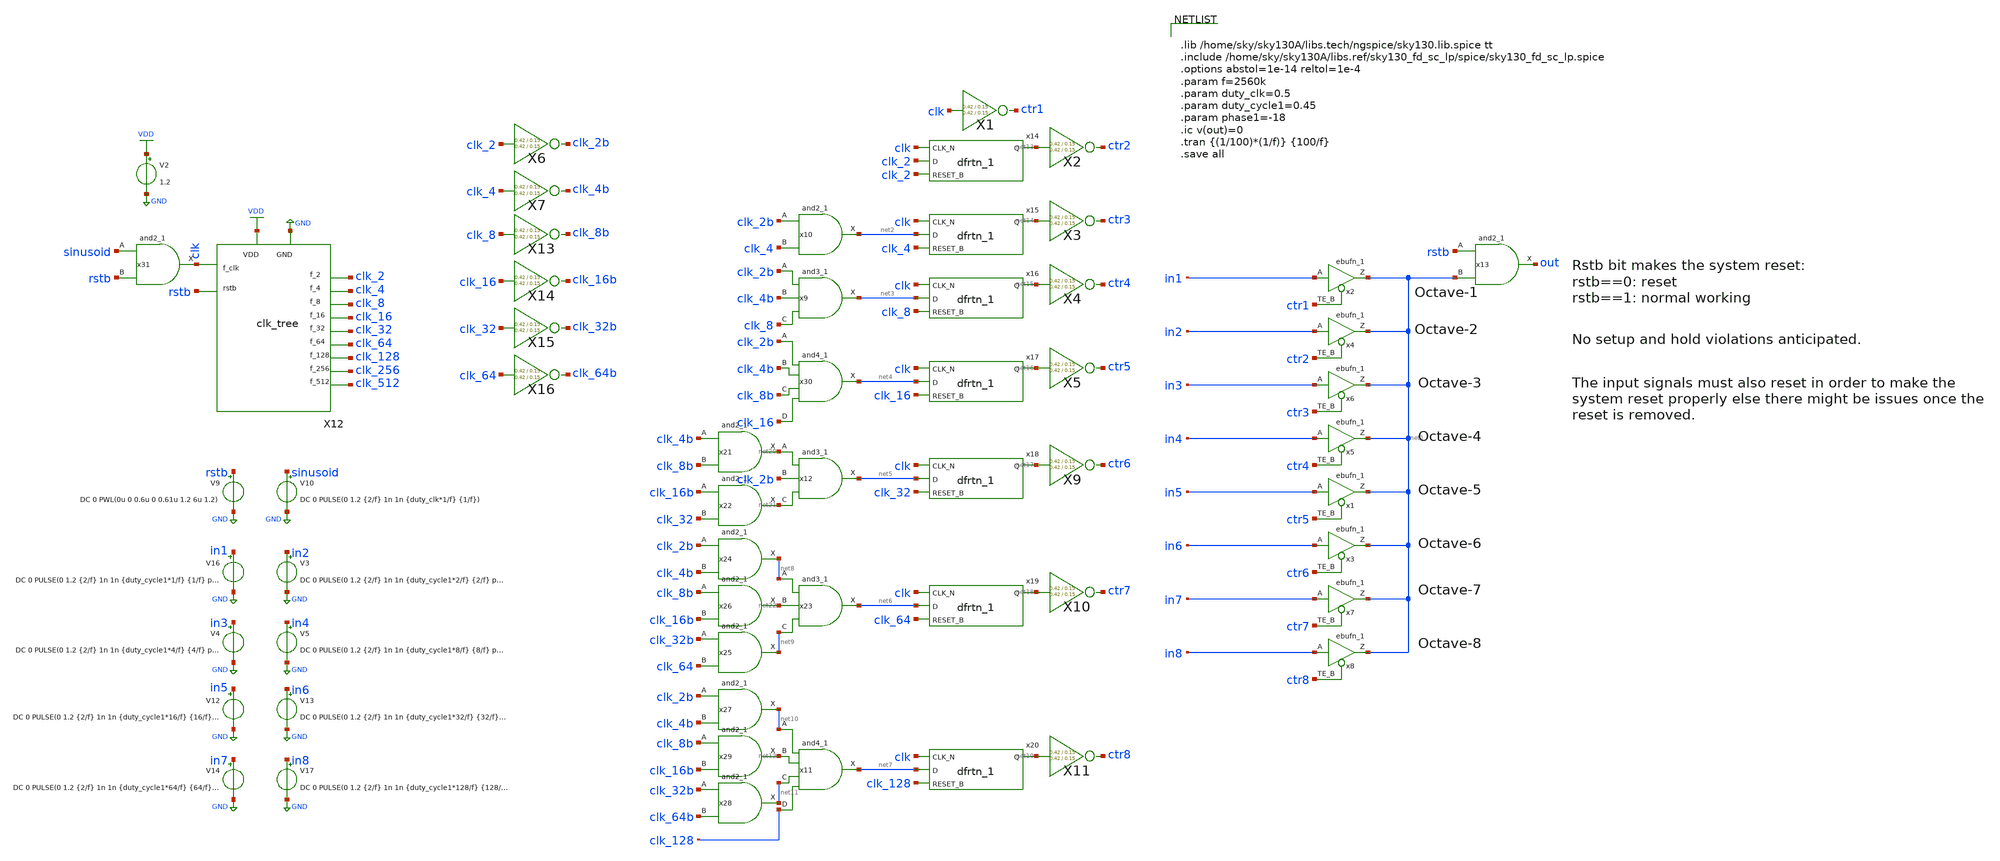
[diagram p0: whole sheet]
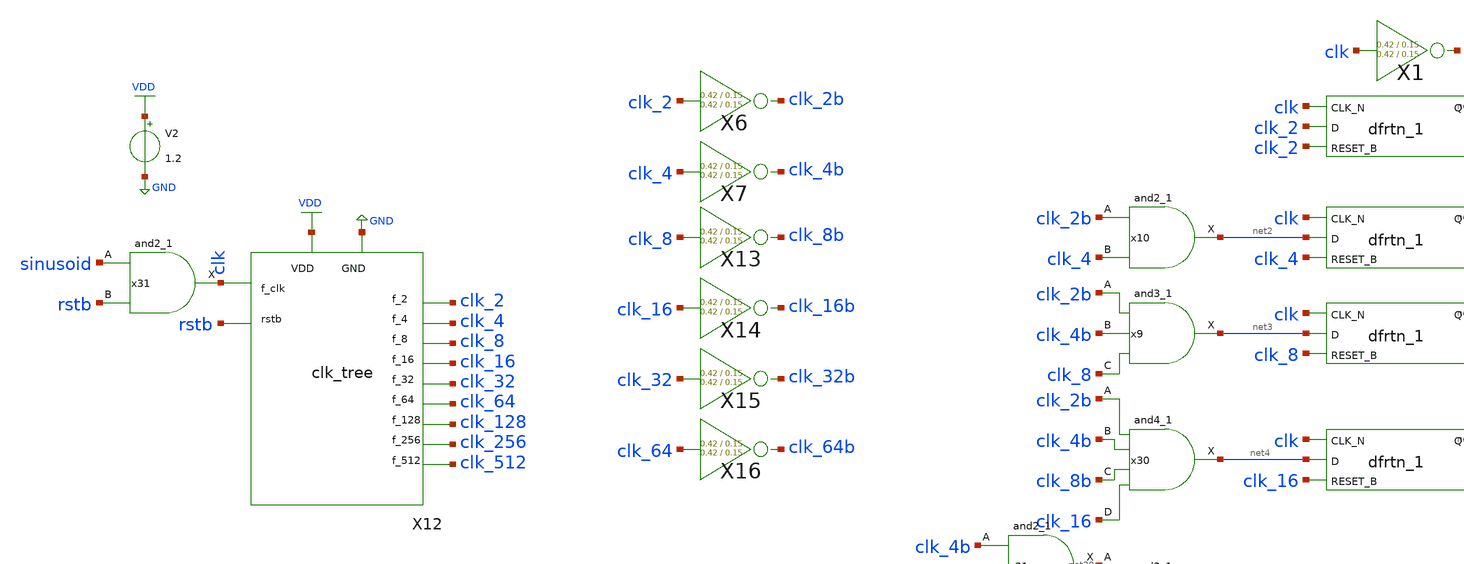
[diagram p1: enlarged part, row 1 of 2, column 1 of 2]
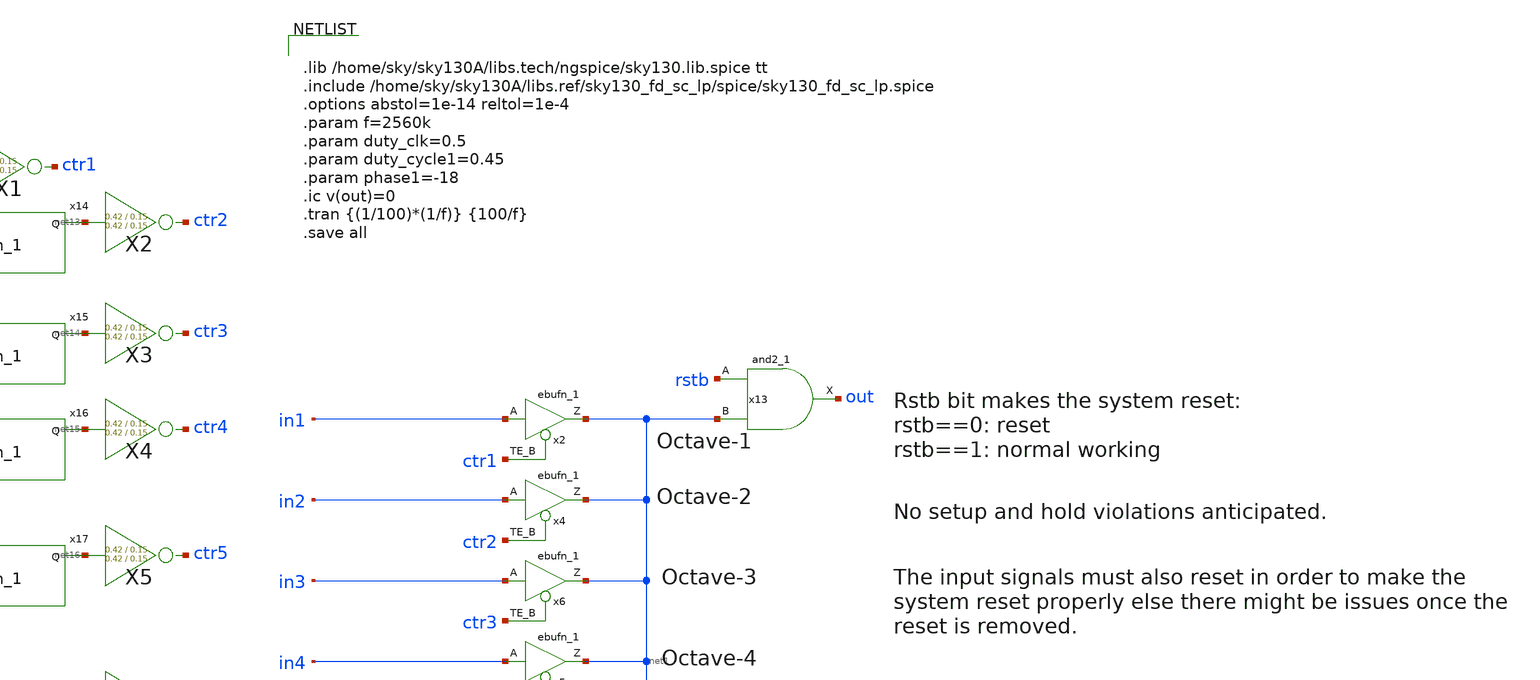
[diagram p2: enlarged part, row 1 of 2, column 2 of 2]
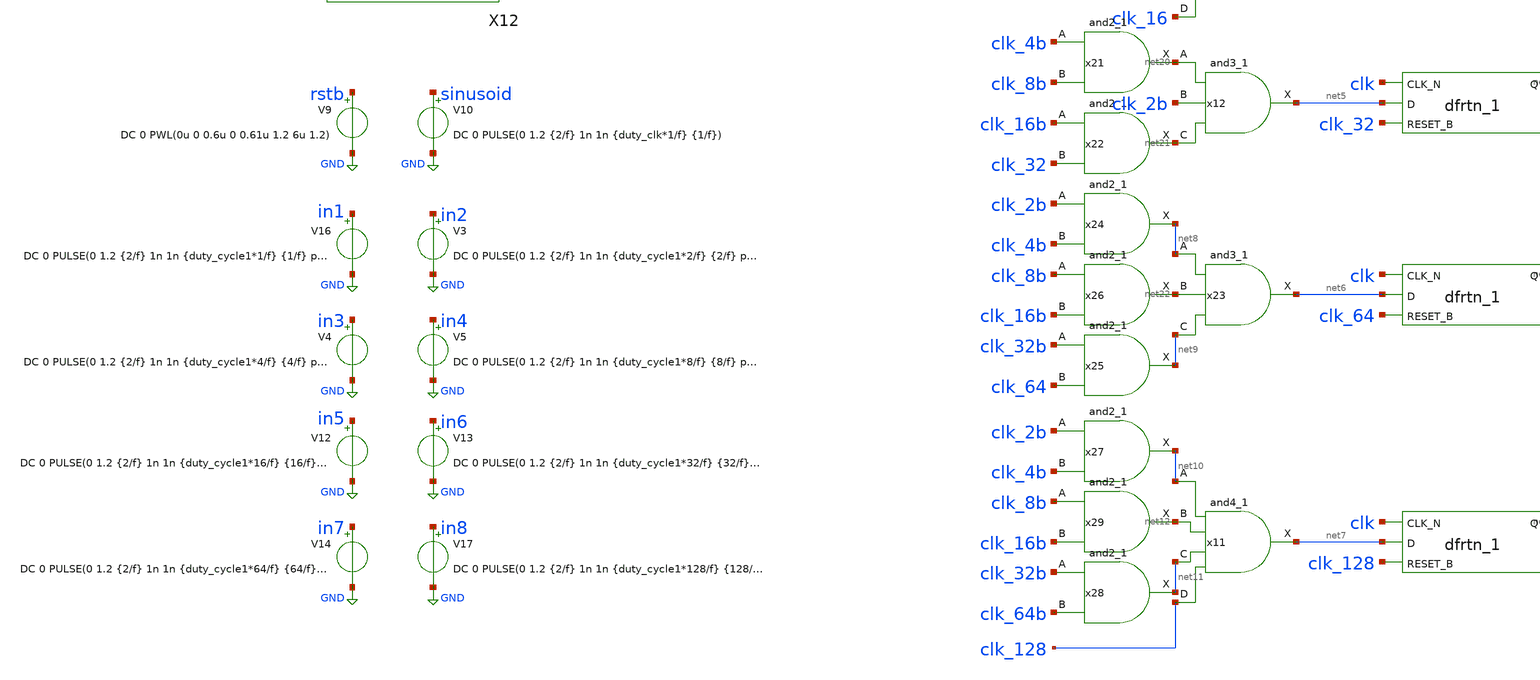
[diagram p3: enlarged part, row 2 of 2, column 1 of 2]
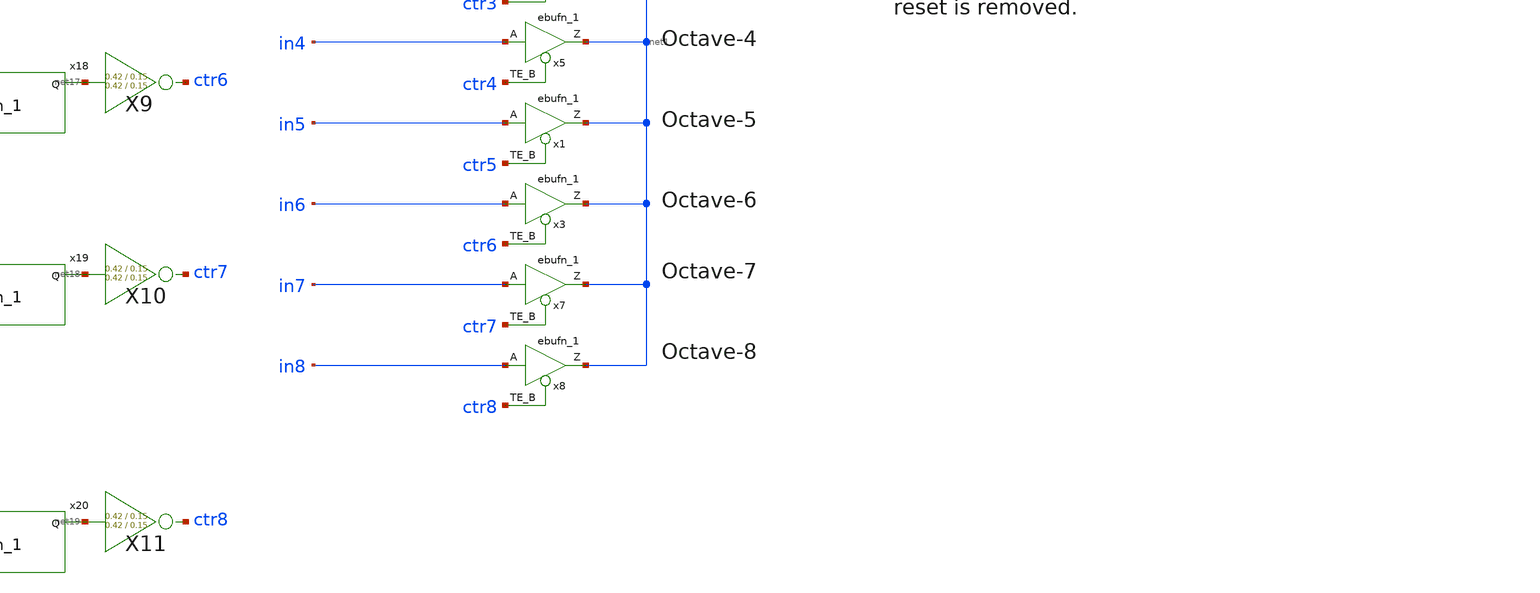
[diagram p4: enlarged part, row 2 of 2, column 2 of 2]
** sch_path: xschem/readout/final_gray_readout.sch
**.subckt final_gray_readout
V2 VDD GND 1.2
V10 sinusoid GND DC 0 PULSE(0 1.2 {2/f} 1n 1n {duty_clk*1/f} {1/f})
x4 in2 ctr2 GND GND VDD VDD net1 sky130_fd_sc_lp__ebufn_1
x6 in3 ctr3 GND GND VDD VDD net1 sky130_fd_sc_lp__ebufn_1
V9 rstb GND DC 0 PWL(0u 0 0.6u 0 0.61u 1.2 6u 1.2)
x2 in1 ctr1 GND GND VDD VDD net1 sky130_fd_sc_lp__ebufn_1
X1 clk ctr1 inv Wpmos=0.42 Lpmos=0.15 Wnmos=0.42 Lnmos=0.15
V16 in1 GND DC 0 PULSE(0 1.2 {2/f} 1n 1n {duty_cycle1*1/f} {1/f} phase1)
V3 in2 GND DC 0 PULSE(0 1.2 {2/f} 1n 1n {duty_cycle1*2/f} {2/f} phase1)
V4 in3 GND DC 0 PULSE(0 1.2 {2/f} 1n 1n {duty_cycle1*4/f} {4/f} phase1)
X6 clk_2 clk_2b inv Wpmos=0.42 Lpmos=0.15 Wnmos=0.42 Lnmos=0.15
X7 clk_4 clk_4b inv Wpmos=0.42 Lpmos=0.15 Wnmos=0.42 Lnmos=0.15
x1 in5 ctr5 GND GND VDD VDD net1 sky130_fd_sc_lp__ebufn_1
x3 in6 ctr6 GND GND VDD VDD net1 sky130_fd_sc_lp__ebufn_1
x5 in4 ctr4 GND GND VDD VDD net1 sky130_fd_sc_lp__ebufn_1
x7 in7 ctr7 GND GND VDD VDD net1 sky130_fd_sc_lp__ebufn_1
x8 in8 ctr8 GND GND VDD VDD net1 sky130_fd_sc_lp__ebufn_1
x10 clk_2b clk_4 GND GND VDD VDD net2 sky130_fd_sc_lp__and2_1
x9 clk_2b clk_4b clk_8 GND GND VDD VDD net3 sky130_fd_sc_lp__and3_1
x11 net10 net12 net11 clk_128 GND GND VDD VDD net7 sky130_fd_sc_lp__and4_1
x13 rstb net1 GND GND VDD VDD out sky130_fd_sc_lp__and2_1
x14 clk clk_2 clk_2 GND GND VDD VDD net13 sky130_fd_sc_lp__dfrtn_1
x15 clk net2 clk_4 GND GND VDD VDD net14 sky130_fd_sc_lp__dfrtn_1
x16 clk net3 clk_8 GND GND VDD VDD net15 sky130_fd_sc_lp__dfrtn_1
x17 clk net4 clk_16 GND GND VDD VDD net16 sky130_fd_sc_lp__dfrtn_1
x18 clk net5 clk_32 GND GND VDD VDD net17 sky130_fd_sc_lp__dfrtn_1
x19 clk net6 clk_64 GND GND VDD VDD net18 sky130_fd_sc_lp__dfrtn_1
x20 clk net7 clk_128 GND GND VDD VDD net19 sky130_fd_sc_lp__dfrtn_1
X2 net13 ctr2 inv Wpmos=0.42 Lpmos=0.15 Wnmos=0.42 Lnmos=0.15
X3 net14 ctr3 inv Wpmos=0.42 Lpmos=0.15 Wnmos=0.42 Lnmos=0.15
X4 net15 ctr4 inv Wpmos=0.42 Lpmos=0.15 Wnmos=0.42 Lnmos=0.15
X5 net16 ctr5 inv Wpmos=0.42 Lpmos=0.15 Wnmos=0.42 Lnmos=0.15
X9 net17 ctr6 inv Wpmos=0.42 Lpmos=0.15 Wnmos=0.42 Lnmos=0.15
X10 net18 ctr7 inv Wpmos=0.42 Lpmos=0.15 Wnmos=0.42 Lnmos=0.15
X11 net19 ctr8 inv Wpmos=0.42 Lpmos=0.15 Wnmos=0.42 Lnmos=0.15
X12 rstb clk clk_2 clk_4 clk_8 clk_16 clk_32 clk_64 clk_128 clk_256 clk_512 VDD GND clk_tree
X13 clk_8 clk_8b inv Wpmos=0.42 Lpmos=0.15 Wnmos=0.42 Lnmos=0.15
X14 clk_16 clk_16b inv Wpmos=0.42 Lpmos=0.15 Wnmos=0.42 Lnmos=0.15
X15 clk_32 clk_32b inv Wpmos=0.42 Lpmos=0.15 Wnmos=0.42 Lnmos=0.15
X16 clk_64 clk_64b inv Wpmos=0.42 Lpmos=0.15 Wnmos=0.42 Lnmos=0.15
V5 in4 GND DC 0 PULSE(0 1.2 {2/f} 1n 1n {duty_cycle1*8/f} {8/f} phase1)
V12 in5 GND DC 0 PULSE(0 1.2 {2/f} 1n 1n {duty_cycle1*16/f} {16/f} phase1)
V13 in6 GND DC 0 PULSE(0 1.2 {2/f} 1n 1n {duty_cycle1*32/f} {32/f} phase1)
V14 in7 GND DC 0 PULSE(0 1.2 {2/f} 1n 1n {duty_cycle1*64/f} {64/f} phase1)
V17 in8 GND DC 0 PULSE(0 1.2 {2/f} 1n 1n {duty_cycle1*128/f} {128/f} phase1)
x12 net20 clk_2b net21 GND GND VDD VDD net5 sky130_fd_sc_lp__and3_1
x21 clk_4b clk_8b GND GND VDD VDD net20 sky130_fd_sc_lp__and2_1
x22 clk_16b clk_32 GND GND VDD VDD net21 sky130_fd_sc_lp__and2_1
x23 net8 net22 net9 GND GND VDD VDD net6 sky130_fd_sc_lp__and3_1
x24 clk_2b clk_4b GND GND VDD VDD net8 sky130_fd_sc_lp__and2_1
x25 clk_32b clk_64 GND GND VDD VDD net9 sky130_fd_sc_lp__and2_1
x26 clk_8b clk_16b GND GND VDD VDD net22 sky130_fd_sc_lp__and2_1
x27 clk_2b clk_4b GND GND VDD VDD net10 sky130_fd_sc_lp__and2_1
x28 clk_32b clk_64b GND GND VDD VDD net11 sky130_fd_sc_lp__and2_1
x29 clk_8b clk_16b GND GND VDD VDD net12 sky130_fd_sc_lp__and2_1
x30 clk_2b clk_4b clk_8b clk_16 GND GND VDD VDD net4 sky130_fd_sc_lp__and4_1
x31 sinusoid rstb GND GND VDD VDD clk sky130_fd_sc_lp__and2_1
**** begin user architecture code


.lib /home/sky/sky130A/libs.tech/ngspice/sky130.lib.spice tt
.include /home/sky/sky130A/libs.ref/sky130_fd_sc_lp/spice/sky130_fd_sc_lp.spice
.options abstol=1e-14 reltol=1e-4
.param f=2560k
.param duty_clk=0.5
.param duty_cycle1=0.45
.param phase1=-18
.ic v(out)=0
.tran {(1/100)*(1/f)} {100/f}
.save all


**** end user architecture code
**.ends

* expanding   symbol:  inv/inv.sym # of pins=2
** sym_path: xschem/inv/inv.sym
** sch_path: xschem/inv/inv.sch
.subckt inv in out  Wpmos=3 Lpmos=0.18 Wnmos=1 Lnmos=0.18
*.ipin in
*.iopin out
XM1 out in GND GND sky130_fd_pr__nfet_01v8 L=Lnmos W=Wnmos nf=1 ad='int((nf+1)/2) * W/nf * 0.29' as='int((nf+2)/2) * W/nf * 0.29'
+ pd='2*int((nf+1)/2) * (W/nf + 0.29)' ps='2*int((nf+2)/2) * (W/nf + 0.29)' nrd='0.29 / W' nrs='0.29 / W'
+ sa=0 sb=0 sd=0 mult=1 m=1
XM2 out in VDD VDD sky130_fd_pr__pfet_01v8 L=Lpmos W=Wpmos nf=1 ad='int((nf+1)/2) * W/nf * 0.29' as='int((nf+2)/2) * W/nf * 0.29'
+ pd='2*int((nf+1)/2) * (W/nf + 0.29)' ps='2*int((nf+2)/2) * (W/nf + 0.29)' nrd='0.29 / W' nrs='0.29 / W'
+ sa=0 sb=0 sd=0 mult=1 m=1
.ends


* expanding   symbol:  clk_tree/clk_tree.sym # of pins=13
** sym_path: xschem/clk_tree/clk_tree.sym
** sch_path: xschem/clk_tree/clk_tree.sch
.subckt clk_tree rstb f_clk f_2 f_4 f_8 f_16 f_32 f_64 f_128 f_256 f_512 VDD GND
*.ipin rstb
*.iopin VDD
*.iopin GND
*.opin f_2
*.opin f_4
*.opin f_8
*.opin f_16
*.opin f_32
*.opin f_64
*.opin f_128
*.opin f_256
*.opin f_512
*.ipin f_clk
x2 f_clk net1 rstb gnd gnd vdd vdd f_2 net1 sky130_fd_sc_lp__dfrbp_1
x4 f_2 net2 rstb gnd gnd vdd vdd f_4 net2 sky130_fd_sc_lp__dfrbp_1
x1 f_4 net3 rstb gnd gnd vdd vdd f_8 net3 sky130_fd_sc_lp__dfrbp_1
x6 f_8 net4 rstb gnd gnd vdd vdd f_16 net4 sky130_fd_sc_lp__dfrbp_1
x7 f_16 net5 rstb gnd gnd vdd vdd f_32 net5 sky130_fd_sc_lp__dfrbp_1
x8 f_32 net6 rstb gnd gnd vdd vdd f_64 net6 sky130_fd_sc_lp__dfrbp_1
x9 f_64 net7 rstb gnd gnd vdd vdd f_128 net7 sky130_fd_sc_lp__dfrbp_1
x14 f_128 net8 rstb gnd gnd vdd vdd f_256 net8 sky130_fd_sc_lp__dfrbp_1
x15 f_256 net9 rstb gnd gnd vdd vdd f_512 net9 sky130_fd_sc_lp__dfrbp_1
.ends

.GLOBAL VDD
.GLOBAL GND
.end
